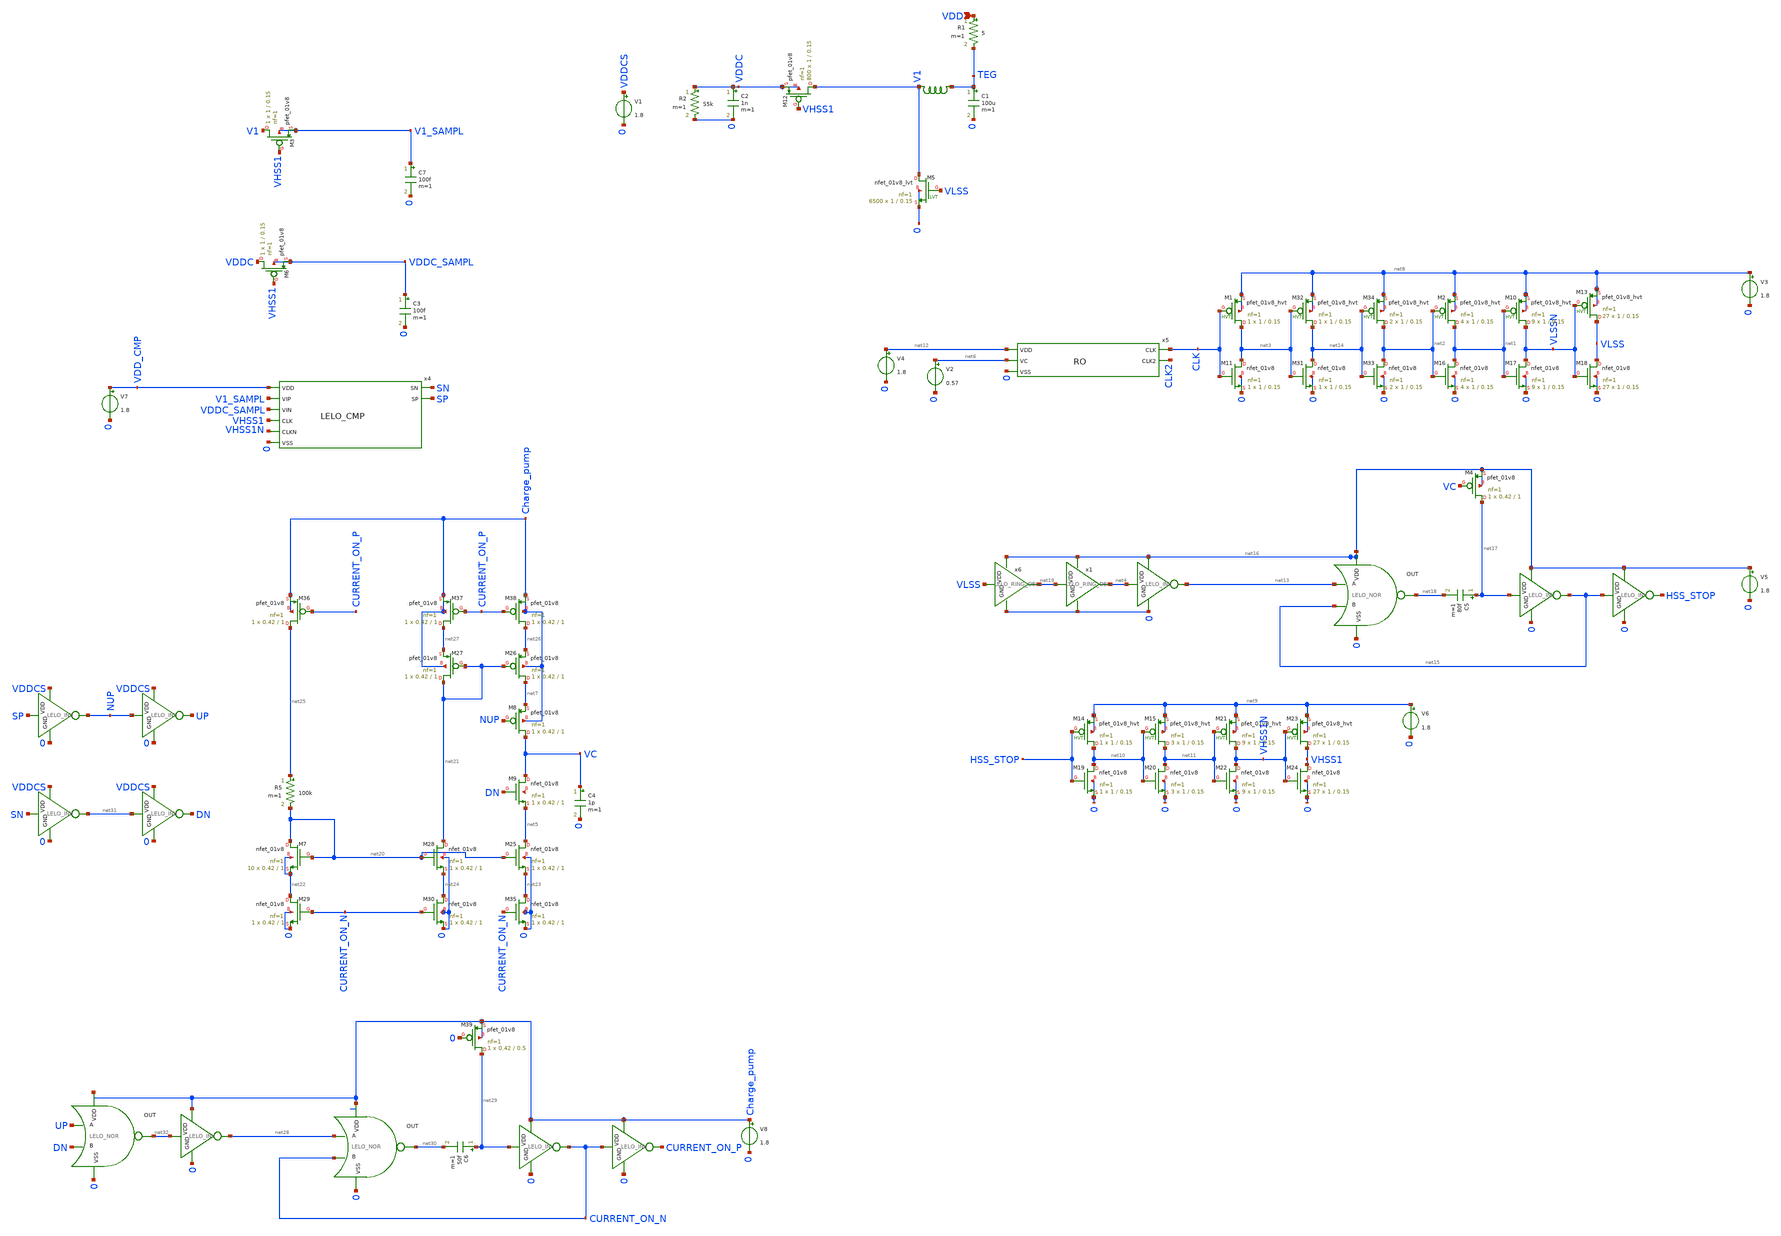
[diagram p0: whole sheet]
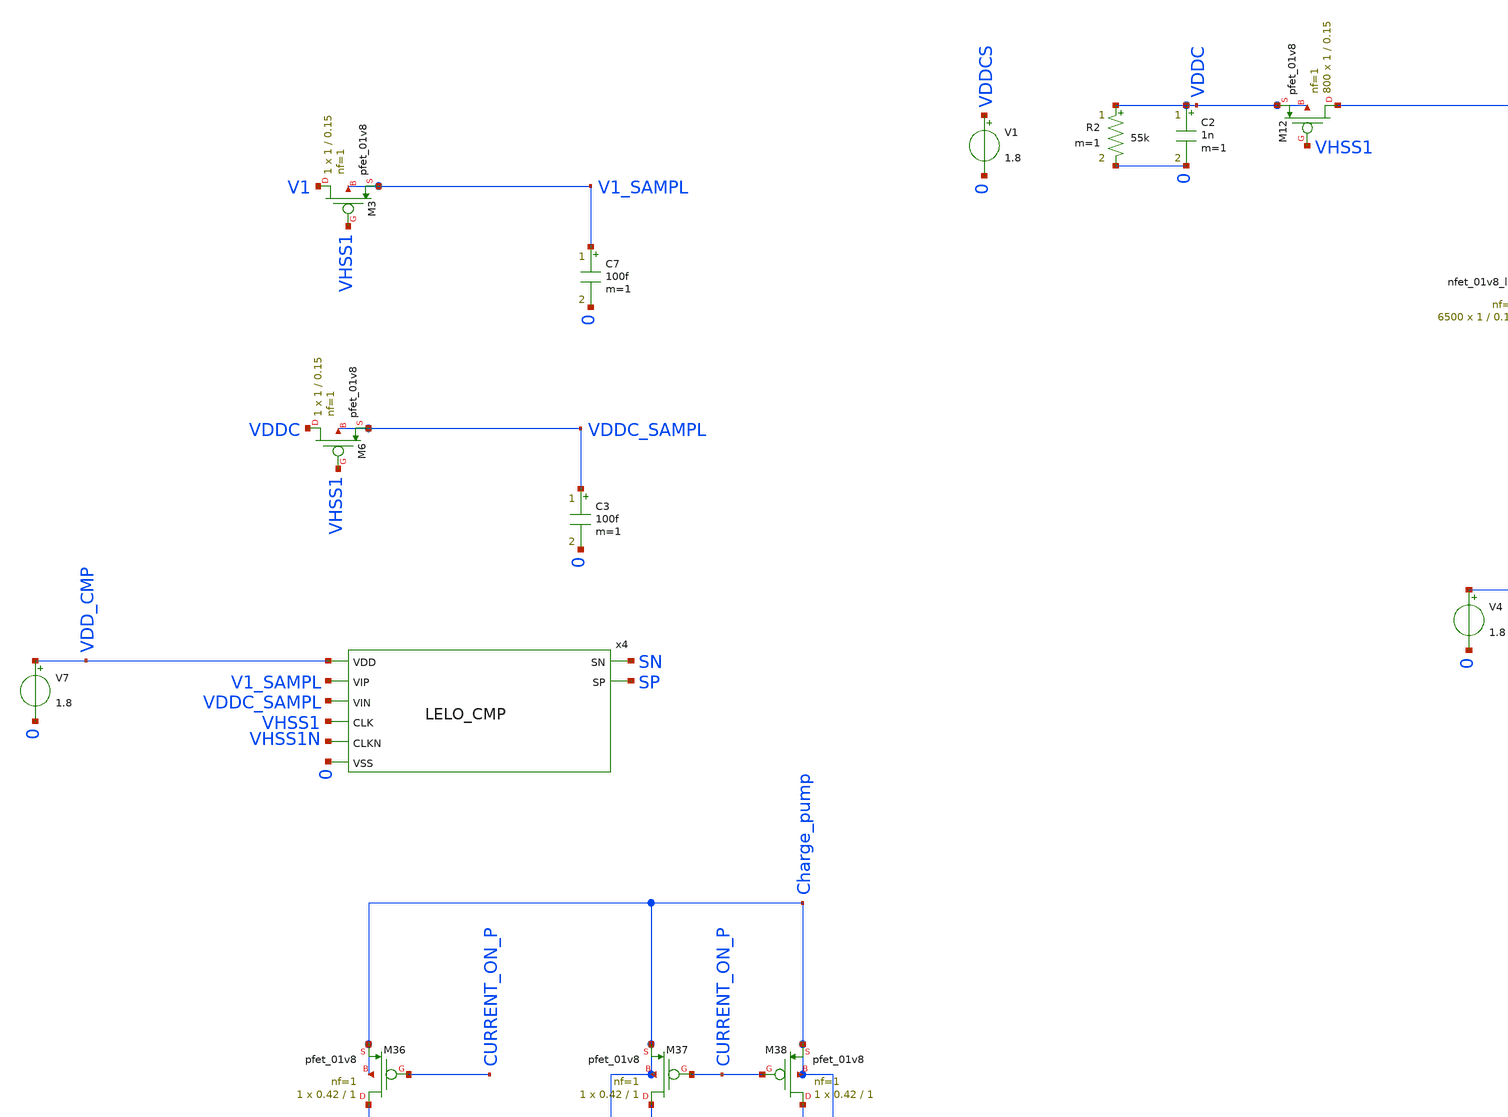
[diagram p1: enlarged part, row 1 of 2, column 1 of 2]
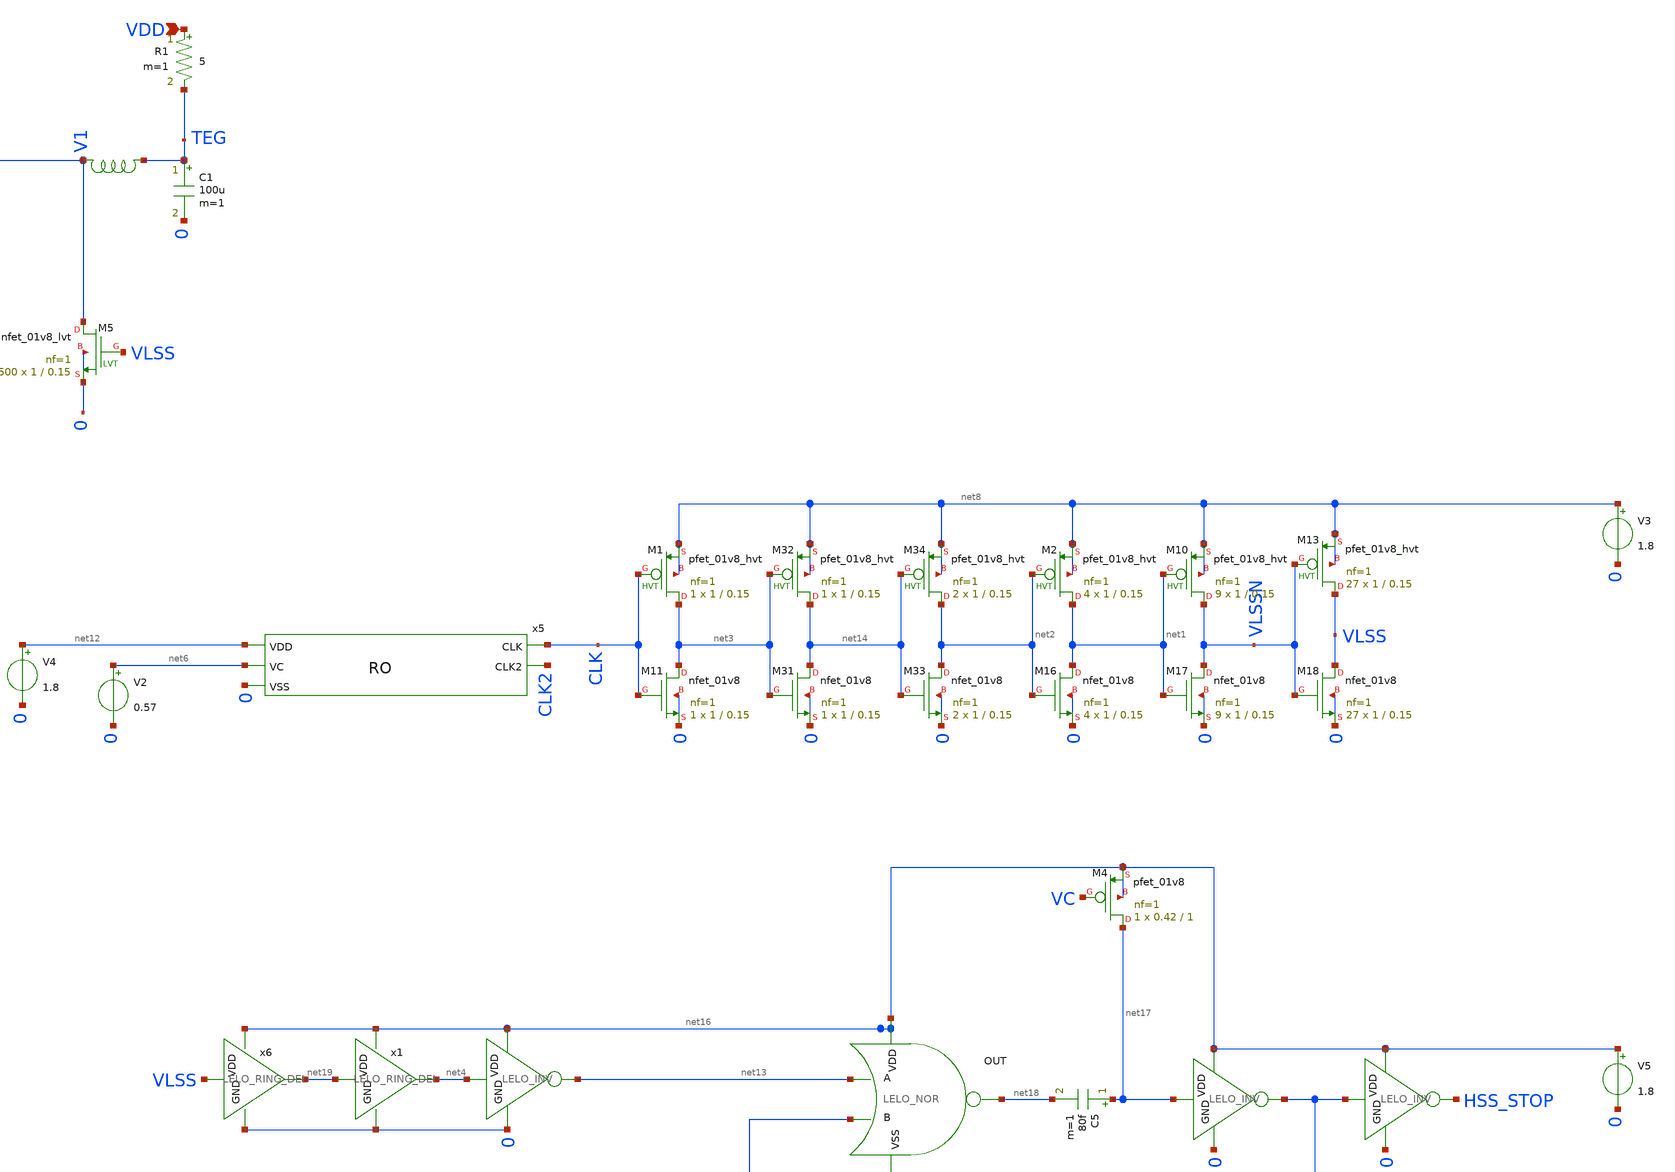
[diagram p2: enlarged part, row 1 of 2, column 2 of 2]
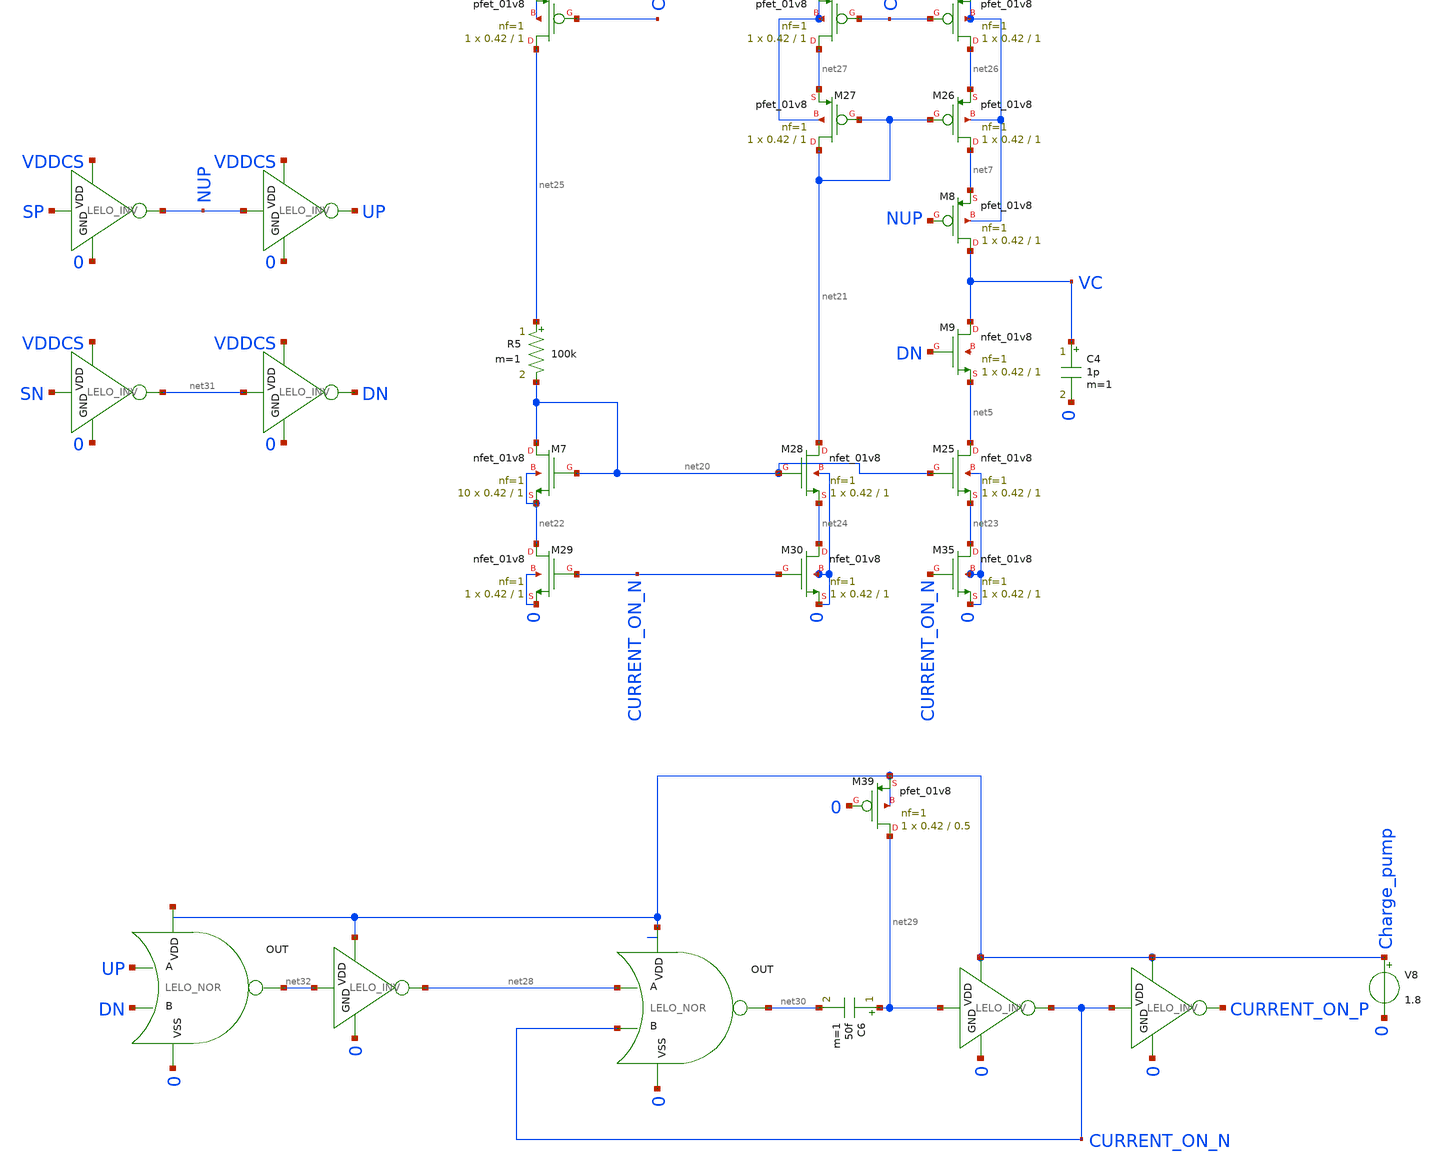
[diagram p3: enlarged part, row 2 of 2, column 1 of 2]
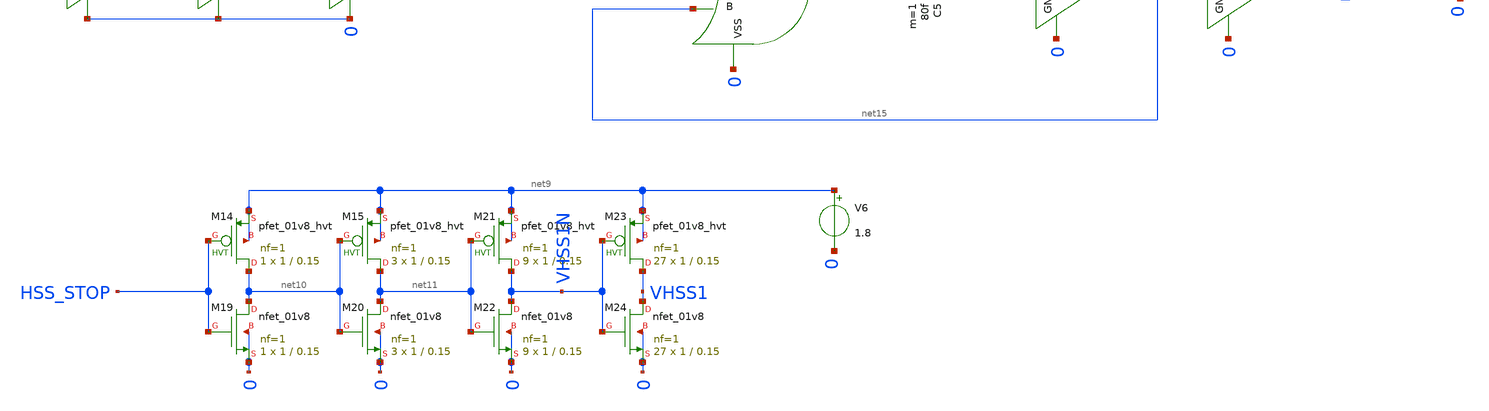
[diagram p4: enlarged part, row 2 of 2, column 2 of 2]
** sch_path: design/LELO_SVOD_SKY130A/LELO_BOOST_STEADY_STATE.sch
**.subckt LELO_BOOST_STEADY_STATE VDD
*.ipin VDD
R1 VDD TEG 5 m=1
C7 V1_SAMPL 0 100f m=1
x5 CLK CLK2 net12 net6 0 RO
XM12 V1 VHSS1 VDDC VDDC sky130_fd_pr__pfet_01v8 L=0.15 W=1 nf=1 ad='int((1 + 1)/2) * 1 / 1 * 0.29' as='int((1 + 2)/2) * 1 / 1 * 0.29'
+ pd='2*int((1 + 1)/2) * (1 / 1 + 0.29)' ps='2*int((1 + 2)/2) * (1 / 1 + 0.29)' nrd='0.29 / 1 ' nrs='0.29 / 1 '
+ sa=0 sb=0 sd=0 mult=800 m=800
x16 net16 net15 HSS_STOP 0 LELO_INV
C1 TEG 0 100u m=1
x9 net16 net4 net13 0 LELO_INV
XM5 V1 VLSS 0 0 sky130_fd_pr__nfet_01v8_lvt L=0.15 W=1 nf=1 ad='int((1 + 1)/2) * 1 / 1 * 0.29' as='int((1 + 2)/2) * 1 / 1 * 0.29'
+ pd='2*int((1 + 1)/2) * (1 / 1 + 0.29)' ps='2*int((1 + 2)/2) * (1 / 1 + 0.29)' nrd='0.29 / 1 ' nrs='0.29 / 1 '
+ sa=0 sb=0 sd=0 mult=6500 m=6500
C2 VDDC 0 1n m=1
V1 VDDCS 0 1.8
R2 VDDC 0 55k m=1
x4 SN SP VDD_CMP V1_SAMPL VDDC_SAMPL VHSS1 VHSS1N 0 LELO_CMP
XM3 V1 VHSS1 V1_SAMPL V1_SAMPL sky130_fd_pr__pfet_01v8 L=0.15 W=1 nf=1 ad='int((1 + 1)/2) * 1 / 1 * 0.29'
+ as='int((1 + 2)/2) * 1 / 1 * 0.29' pd='2*int((1 + 1)/2) * (1 / 1 + 0.29)' ps='2*int((1 + 2)/2) * (1 / 1 + 0.29)'
+ nrd='0.29 / 1 ' nrs='0.29 / 1 ' sa=0 sb=0 sd=0 mult=1 m=1
C3 VDDC_SAMPL 0 100f m=1
XM6 VDDC VHSS1 VDDC_SAMPL VDDC_SAMPL sky130_fd_pr__pfet_01v8 L=0.15 W=1 nf=1 ad='int((1 + 1)/2) * 1 / 1 * 0.29'
+ as='int((1 + 2)/2) * 1 / 1 * 0.29' pd='2*int((1 + 1)/2) * (1 / 1 + 0.29)' ps='2*int((1 + 2)/2) * (1 / 1 + 0.29)'
+ nrd='0.29 / 1 ' nrs='0.29 / 1 ' sa=0 sb=0 sd=0 mult=1 m=1
C4 VC 0 1p m=1
XM8 VC NUP net7 Charge_pump sky130_fd_pr__pfet_01v8 L=1 W=0.42 nf=1 ad='int((1 + 1)/2) * 0.42 / 1 * 0.29'
+ as='int((1 + 2)/2) * 0.42 / 1 * 0.29' pd='2*int((1 + 1)/2) * (0.42 / 1 + 0.29)' ps='2*int((1 + 2)/2) * (0.42 / 1 + 0.29)'
+ nrd='0.29 / 0.42 ' nrs='0.29 / 0.42 ' sa=0 sb=0 sd=0 mult=1 m=1
XM9 VC DN net5 net33 sky130_fd_pr__nfet_01v8 L=1 W=0.42 nf=1 ad='int((1 + 1)/2) * 0.42 / 1 * 0.29' as='int((1 + 2)/2) * 0.42 / 1 * 0.29'
+ pd='2*int((1 + 1)/2) * (0.42 / 1 + 0.29)' ps='2*int((1 + 2)/2) * (0.42 / 1 + 0.29)' nrd='0.29 / 0.42 '
+ nrs='0.29 / 0.42 ' sa=0 sb=0 sd=0 mult=1 m=1
V2 net6 0 0.57
XM11 net3 CLK 0 0 sky130_fd_pr__nfet_01v8 L=0.15 W=1 nf=1 ad='int((1 + 1)/2) * 1 / 1 * 0.29' as='int((1 + 2)/2) * 1 / 1 * 0.29'
+ pd='2*int((1 + 1)/2) * (1 / 1 + 0.29)' ps='2*int((1 + 2)/2) * (1 / 1 + 0.29)' nrd='0.29 / 1 ' nrs='0.29 / 1 '
+ sa=0 sb=0 sd=0 mult=1 m=1
XM16 net1 net2 0 0 sky130_fd_pr__nfet_01v8 L=0.15 W=1 nf=1 ad='int((1 + 1)/2) * 1 / 1 * 0.29' as='int((1 + 2)/2) * 1 / 1 * 0.29'
+ pd='2*int((1 + 1)/2) * (1 / 1 + 0.29)' ps='2*int((1 + 2)/2) * (1 / 1 + 0.29)' nrd='0.29 / 1 ' nrs='0.29 / 1 '
+ sa=0 sb=0 sd=0 mult=4 m=4
XM17 VLSSN net1 0 0 sky130_fd_pr__nfet_01v8 L=0.15 W=1 nf=1 ad='int((1 + 1)/2) * 1 / 1 * 0.29' as='int((1 + 2)/2) * 1 / 1 * 0.29'
+ pd='2*int((1 + 1)/2) * (1 / 1 + 0.29)' ps='2*int((1 + 2)/2) * (1 / 1 + 0.29)' nrd='0.29 / 1 ' nrs='0.29 / 1 '
+ sa=0 sb=0 sd=0 mult=9 m=9
XM18 VLSS VLSSN 0 0 sky130_fd_pr__nfet_01v8 L=0.15 W=1 nf=1 ad='int((1 + 1)/2) * 1 / 1 * 0.29' as='int((1 + 2)/2) * 1 / 1 * 0.29'
+ pd='2*int((1 + 1)/2) * (1 / 1 + 0.29)' ps='2*int((1 + 2)/2) * (1 / 1 + 0.29)' nrd='0.29 / 1 ' nrs='0.29 / 1 '
+ sa=0 sb=0 sd=0 mult=27 m=27
XM19 net10 HSS_STOP 0 0 sky130_fd_pr__nfet_01v8 L=0.15 W=1 nf=1 ad='int((1 + 1)/2) * 1 / 1 * 0.29' as='int((1 + 2)/2) * 1 / 1 * 0.29'
+ pd='2*int((1 + 1)/2) * (1 / 1 + 0.29)' ps='2*int((1 + 2)/2) * (1 / 1 + 0.29)' nrd='0.29 / 1 ' nrs='0.29 / 1 '
+ sa=0 sb=0 sd=0 mult=1 m=1
XM20 net11 net10 0 0 sky130_fd_pr__nfet_01v8 L=0.15 W=1 nf=1 ad='int((1 + 1)/2) * 1 / 1 * 0.29' as='int((1 + 2)/2) * 1 / 1 * 0.29'
+ pd='2*int((1 + 1)/2) * (1 / 1 + 0.29)' ps='2*int((1 + 2)/2) * (1 / 1 + 0.29)' nrd='0.29 / 1 ' nrs='0.29 / 1 '
+ sa=0 sb=0 sd=0 mult=3 m=3
XM22 VHSS1N net11 0 0 sky130_fd_pr__nfet_01v8 L=0.15 W=1 nf=1 ad='int((1 + 1)/2) * 1 / 1 * 0.29' as='int((1 + 2)/2) * 1 / 1 * 0.29'
+ pd='2*int((1 + 1)/2) * (1 / 1 + 0.29)' ps='2*int((1 + 2)/2) * (1 / 1 + 0.29)' nrd='0.29 / 1 ' nrs='0.29 / 1 '
+ sa=0 sb=0 sd=0 mult=9 m=9
XM24 VHSS1 VHSS1N 0 0 sky130_fd_pr__nfet_01v8 L=0.15 W=1 nf=1 ad='int((1 + 1)/2) * 1 / 1 * 0.29' as='int((1 + 2)/2) * 1 / 1 * 0.29'
+ pd='2*int((1 + 1)/2) * (1 / 1 + 0.29)' ps='2*int((1 + 2)/2) * (1 / 1 + 0.29)' nrd='0.29 / 1 ' nrs='0.29 / 1 '
+ sa=0 sb=0 sd=0 mult=27 m=27
XM1 net3 CLK net8 net8 sky130_fd_pr__pfet_01v8_hvt L=0.15 W=1 nf=1 ad='int((1 + 1)/2) * 1 / 1 * 0.29'
+ as='int((1 + 2)/2) * 1 / 1 * 0.29' pd='2*int((1 + 1)/2) * (1 / 1 + 0.29)' ps='2*int((1 + 2)/2) * (1 / 1 + 0.29)'
+ nrd='0.29 / 1 ' nrs='0.29 / 1 ' sa=0 sb=0 sd=0 mult=1 m=1
XM2 net1 net2 net8 net8 sky130_fd_pr__pfet_01v8_hvt L=0.15 W=1 nf=1 ad='int((1 + 1)/2) * 1 / 1 * 0.29'
+ as='int((1 + 2)/2) * 1 / 1 * 0.29' pd='2*int((1 + 1)/2) * (1 / 1 + 0.29)' ps='2*int((1 + 2)/2) * (1 / 1 + 0.29)'
+ nrd='0.29 / 1 ' nrs='0.29 / 1 ' sa=0 sb=0 sd=0 mult=4 m=4
XM10 VLSSN net1 net8 net8 sky130_fd_pr__pfet_01v8_hvt L=0.15 W=1 nf=1 ad='int((1 + 1)/2) * 1 / 1 * 0.29'
+ as='int((1 + 2)/2) * 1 / 1 * 0.29' pd='2*int((1 + 1)/2) * (1 / 1 + 0.29)' ps='2*int((1 + 2)/2) * (1 / 1 + 0.29)'
+ nrd='0.29 / 1 ' nrs='0.29 / 1 ' sa=0 sb=0 sd=0 mult=9 m=9
XM13 VLSS VLSSN net8 net8 sky130_fd_pr__pfet_01v8_hvt L=0.15 W=1 nf=1 ad='int((1 + 1)/2) * 1 / 1 * 0.29'
+ as='int((1 + 2)/2) * 1 / 1 * 0.29' pd='2*int((1 + 1)/2) * (1 / 1 + 0.29)' ps='2*int((1 + 2)/2) * (1 / 1 + 0.29)'
+ nrd='0.29 / 1 ' nrs='0.29 / 1 ' sa=0 sb=0 sd=0 mult=27 m=27
XM14 net10 HSS_STOP net9 net9 sky130_fd_pr__pfet_01v8_hvt L=0.15 W=1 nf=1 ad='int((1 + 1)/2) * 1 / 1 * 0.29'
+ as='int((1 + 2)/2) * 1 / 1 * 0.29' pd='2*int((1 + 1)/2) * (1 / 1 + 0.29)' ps='2*int((1 + 2)/2) * (1 / 1 + 0.29)'
+ nrd='0.29 / 1 ' nrs='0.29 / 1 ' sa=0 sb=0 sd=0 mult=1 m=1
XM15 net11 net10 net9 net9 sky130_fd_pr__pfet_01v8_hvt L=0.15 W=1 nf=1 ad='int((1 + 1)/2) * 1 / 1 * 0.29'
+ as='int((1 + 2)/2) * 1 / 1 * 0.29' pd='2*int((1 + 1)/2) * (1 / 1 + 0.29)' ps='2*int((1 + 2)/2) * (1 / 1 + 0.29)'
+ nrd='0.29 / 1 ' nrs='0.29 / 1 ' sa=0 sb=0 sd=0 mult=3 m=3
XM21 VHSS1N net11 net9 net9 sky130_fd_pr__pfet_01v8_hvt L=0.15 W=1 nf=1 ad='int((1 + 1)/2) * 1 / 1 * 0.29'
+ as='int((1 + 2)/2) * 1 / 1 * 0.29' pd='2*int((1 + 1)/2) * (1 / 1 + 0.29)' ps='2*int((1 + 2)/2) * (1 / 1 + 0.29)'
+ nrd='0.29 / 1 ' nrs='0.29 / 1 ' sa=0 sb=0 sd=0 mult=9 m=9
XM23 VHSS1 VHSS1N net9 net9 sky130_fd_pr__pfet_01v8_hvt L=0.15 W=1 nf=1 ad='int((1 + 1)/2) * 1 / 1 * 0.29'
+ as='int((1 + 2)/2) * 1 / 1 * 0.29' pd='2*int((1 + 1)/2) * (1 / 1 + 0.29)' ps='2*int((1 + 2)/2) * (1 / 1 + 0.29)'
+ nrd='0.29 / 1 ' nrs='0.29 / 1 ' sa=0 sb=0 sd=0 mult=27 m=27
V4 net12 0 1.8
V3 net8 0 1.8
V5 net16 0 1.8
V6 net9 0 1.8
V7 VDD_CMP 0 1.8
XM31 net14 net3 0 0 sky130_fd_pr__nfet_01v8 L=0.15 W=1 nf=1 ad='int((1 + 1)/2) * 1 / 1 * 0.29' as='int((1 + 2)/2) * 1 / 1 * 0.29'
+ pd='2*int((1 + 1)/2) * (1 / 1 + 0.29)' ps='2*int((1 + 2)/2) * (1 / 1 + 0.29)' nrd='0.29 / 1 ' nrs='0.29 / 1 '
+ sa=0 sb=0 sd=0 mult=1 m=1
XM32 net14 net3 net8 net8 sky130_fd_pr__pfet_01v8_hvt L=0.15 W=1 nf=1 ad='int((1 + 1)/2) * 1 / 1 * 0.29'
+ as='int((1 + 2)/2) * 1 / 1 * 0.29' pd='2*int((1 + 1)/2) * (1 / 1 + 0.29)' ps='2*int((1 + 2)/2) * (1 / 1 + 0.29)'
+ nrd='0.29 / 1 ' nrs='0.29 / 1 ' sa=0 sb=0 sd=0 mult=1 m=1
XM33 net2 net14 0 0 sky130_fd_pr__nfet_01v8 L=0.15 W=1 nf=1 ad='int((1 + 1)/2) * 1 / 1 * 0.29' as='int((1 + 2)/2) * 1 / 1 * 0.29'
+ pd='2*int((1 + 1)/2) * (1 / 1 + 0.29)' ps='2*int((1 + 2)/2) * (1 / 1 + 0.29)' nrd='0.29 / 1 ' nrs='0.29 / 1 '
+ sa=0 sb=0 sd=0 mult=2 m=2
XM34 net2 net14 net8 net8 sky130_fd_pr__pfet_01v8_hvt L=0.15 W=1 nf=1 ad='int((1 + 1)/2) * 1 / 1 * 0.29'
+ as='int((1 + 2)/2) * 1 / 1 * 0.29' pd='2*int((1 + 1)/2) * (1 / 1 + 0.29)' ps='2*int((1 + 2)/2) * (1 / 1 + 0.29)'
+ nrd='0.29 / 1 ' nrs='0.29 / 1 ' sa=0 sb=0 sd=0 mult=2 m=2
x7 TEG V1 XGL6030-822_sat
x10 VDDCS SP NUP 0 LELO_INV
x2 net16 net18 net13 net15 0 LELO_NOR
C5 net17 net18 80f m=1
x3 net16 net17 net15 0 LELO_INV
XM4 net17 VC net16 net16 sky130_fd_pr__pfet_01v8 L=1 W=0.42 nf=1 ad='int((1 + 1)/2) * 0.42 / 1 * 0.29'
+ as='int((1 + 2)/2) * 0.42 / 1 * 0.29' pd='2*int((1 + 1)/2) * (0.42 / 1 + 0.29)' ps='2*int((1 + 2)/2) * (0.42 / 1 + 0.29)'
+ nrd='0.29 / 0.42 ' nrs='0.29 / 0.42 ' sa=0 sb=0 sd=0 mult=1 m=1
x1 net16 net19 net4 0 LELO_RING_DEL
x6 net16 VLSS net19 0 LELO_RING_DEL
R5 net25 net20 100k m=1
XM7 net20 net20 net22 net22 sky130_fd_pr__nfet_01v8 L=1 W=0.42 nf=1 ad='int((1 + 1)/2) * 0.42 / 1 * 0.29'
+ as='int((1 + 2)/2) * 0.42 / 1 * 0.29' pd='2*int((1 + 1)/2) * (0.42 / 1 + 0.29)' ps='2*int((1 + 2)/2) * (0.42 / 1 + 0.29)'
+ nrd='0.29 / 0.42 ' nrs='0.29 / 0.42 ' sa=0 sb=0 sd=0 mult=10 m=10
XM25 net5 net20 net23 0 sky130_fd_pr__nfet_01v8 L=1 W=0.42 nf=1 ad='int((1 + 1)/2) * 0.42 / 1 * 0.29'
+ as='int((1 + 2)/2) * 0.42 / 1 * 0.29' pd='2*int((1 + 1)/2) * (0.42 / 1 + 0.29)' ps='2*int((1 + 2)/2) * (0.42 / 1 + 0.29)'
+ nrd='0.29 / 0.42 ' nrs='0.29 / 0.42 ' sa=0 sb=0 sd=0 mult=1 m=1
XM26 net7 net21 net26 Charge_pump sky130_fd_pr__pfet_01v8 L=1 W=0.42 nf=1 ad='int((1 + 1)/2) * 0.42 / 1 * 0.29'
+ as='int((1 + 2)/2) * 0.42 / 1 * 0.29' pd='2*int((1 + 1)/2) * (0.42 / 1 + 0.29)' ps='2*int((1 + 2)/2) * (0.42 / 1 + 0.29)'
+ nrd='0.29 / 0.42 ' nrs='0.29 / 0.42 ' sa=0 sb=0 sd=0 mult=1 m=1
XM27 net21 net21 net27 Charge_pump sky130_fd_pr__pfet_01v8 L=1 W=0.42 nf=1 ad='int((1 + 1)/2) * 0.42 / 1 * 0.29'
+ as='int((1 + 2)/2) * 0.42 / 1 * 0.29' pd='2*int((1 + 1)/2) * (0.42 / 1 + 0.29)' ps='2*int((1 + 2)/2) * (0.42 / 1 + 0.29)'
+ nrd='0.29 / 0.42 ' nrs='0.29 / 0.42 ' sa=0 sb=0 sd=0 mult=1 m=1
XM28 net21 net20 net24 0 sky130_fd_pr__nfet_01v8 L=1 W=0.42 nf=1 ad='int((1 + 1)/2) * 0.42 / 1 * 0.29'
+ as='int((1 + 2)/2) * 0.42 / 1 * 0.29' pd='2*int((1 + 1)/2) * (0.42 / 1 + 0.29)' ps='2*int((1 + 2)/2) * (0.42 / 1 + 0.29)'
+ nrd='0.29 / 0.42 ' nrs='0.29 / 0.42 ' sa=0 sb=0 sd=0 mult=1 m=1
XM29 net22 CURRENT_ON_N 0 0 sky130_fd_pr__nfet_01v8 L=1 W=0.42 nf=1 ad='int((1 + 1)/2) * 0.42 / 1 * 0.29'
+ as='int((1 + 2)/2) * 0.42 / 1 * 0.29' pd='2*int((1 + 1)/2) * (0.42 / 1 + 0.29)' ps='2*int((1 + 2)/2) * (0.42 / 1 + 0.29)'
+ nrd='0.29 / 0.42 ' nrs='0.29 / 0.42 ' sa=0 sb=0 sd=0 mult=1 m=1
XM30 net24 CURRENT_ON_N 0 0 sky130_fd_pr__nfet_01v8 L=1 W=0.42 nf=1 ad='int((1 + 1)/2) * 0.42 / 1 * 0.29'
+ as='int((1 + 2)/2) * 0.42 / 1 * 0.29' pd='2*int((1 + 1)/2) * (0.42 / 1 + 0.29)' ps='2*int((1 + 2)/2) * (0.42 / 1 + 0.29)'
+ nrd='0.29 / 0.42 ' nrs='0.29 / 0.42 ' sa=0 sb=0 sd=0 mult=1 m=1
XM35 net23 CURRENT_ON_N 0 0 sky130_fd_pr__nfet_01v8 L=1 W=0.42 nf=1 ad='int((1 + 1)/2) * 0.42 / 1 * 0.29'
+ as='int((1 + 2)/2) * 0.42 / 1 * 0.29' pd='2*int((1 + 1)/2) * (0.42 / 1 + 0.29)' ps='2*int((1 + 2)/2) * (0.42 / 1 + 0.29)'
+ nrd='0.29 / 0.42 ' nrs='0.29 / 0.42 ' sa=0 sb=0 sd=0 mult=1 m=1
XM36 net25 CURRENT_ON_P Charge_pump Charge_pump sky130_fd_pr__pfet_01v8 L=1 W=0.42 nf=1 ad='int((1 + 1)/2) * 0.42 / 1 * 0.29'
+ as='int((1 + 2)/2) * 0.42 / 1 * 0.29' pd='2*int((1 + 1)/2) * (0.42 / 1 + 0.29)' ps='2*int((1 + 2)/2) * (0.42 / 1 + 0.29)'
+ nrd='0.29 / 0.42 ' nrs='0.29 / 0.42 ' sa=0 sb=0 sd=0 mult=1 m=1
XM37 net27 CURRENT_ON_P Charge_pump Charge_pump sky130_fd_pr__pfet_01v8 L=1 W=0.42 nf=1 ad='int((1 + 1)/2) * 0.42 / 1 * 0.29'
+ as='int((1 + 2)/2) * 0.42 / 1 * 0.29' pd='2*int((1 + 1)/2) * (0.42 / 1 + 0.29)' ps='2*int((1 + 2)/2) * (0.42 / 1 + 0.29)'
+ nrd='0.29 / 0.42 ' nrs='0.29 / 0.42 ' sa=0 sb=0 sd=0 mult=1 m=1
XM38 net26 CURRENT_ON_P Charge_pump Charge_pump sky130_fd_pr__pfet_01v8 L=1 W=0.42 nf=1 ad='int((1 + 1)/2) * 0.42 / 1 * 0.29'
+ as='int((1 + 2)/2) * 0.42 / 1 * 0.29' pd='2*int((1 + 1)/2) * (0.42 / 1 + 0.29)' ps='2*int((1 + 2)/2) * (0.42 / 1 + 0.29)'
+ nrd='0.29 / 0.42 ' nrs='0.29 / 0.42 ' sa=0 sb=0 sd=0 mult=1 m=1
x8 Charge_pump CURRENT_ON_N CURRENT_ON_P 0 LELO_INV
V8 Charge_pump 0 1.8
x12 Charge_pump net30 net28 CURRENT_ON_N 0 LELO_NOR
C6 net29 net30 50f m=1
x13 Charge_pump net29 CURRENT_ON_N 0 LELO_INV
XM39 net29 0 Charge_pump Charge_pump sky130_fd_pr__pfet_01v8 L=0.5 W=0.42 nf=1 ad='int((1 + 1)/2) * 0.42 / 1 * 0.29'
+ as='int((1 + 2)/2) * 0.42 / 1 * 0.29' pd='2*int((1 + 1)/2) * (0.42 / 1 + 0.29)' ps='2*int((1 + 2)/2) * (0.42 / 1 + 0.29)'
+ nrd='0.29 / 0.42 ' nrs='0.29 / 0.42 ' sa=0 sb=0 sd=0 mult=1 m=1
x11 VDDCS SN net31 0 LELO_INV
x14 VDDCS net31 DN 0 LELO_INV
x15 net34 net32 UP DN 0 LELO_NOR
x17 VDDCS NUP UP 0 LELO_INV
x18 Charge_pump net32 net28 0 LELO_INV
**.ends

* expanding   symbol:  LELO_SVOD_SKY130A/RO.sym # of pins=5
** sym_path: design/LELO_SVOD_SKY130A/RO.sym
** sch_path: design/LELO_SVOD_SKY130A/RO.sch
.subckt RO CLK CLK2 VDD VC VSS
*.opin CLK
*.ipin VSS
*.opin CLK2
*.ipin VDD
*.ipin VC
x1 VDD VC2 CLK net1 VC VSS LELO_RING_DEL_VC
x2 VDD VC2 net1 net2 VC VSS LELO_RING_DEL_VC
x3 VDD VC2 net2 net3 VC VSS LELO_RING_DEL_VC
x4 VDD VC2 net3 CLK2 VC VSS LELO_RING_DEL_VC
x5 VDD VC2 CLK2 net4 VC VSS LELO_RING_DEL_VC
x6 VDD VC2 net4 net5 VC VSS LELO_RING_DEL_VC
x7 VDD VC2 net5 CLK VC VSS LELO_RING_DEL_VC
XM1 VC2 VC VSS VSS sky130_fd_pr__nfet_01v8 L=5 W=0.42 nf=1 ad='int((1 + 1)/2) * 0.42 / 1 * 0.29' as='int((1 + 2)/2) * 0.42 / 1 * 0.29'
+ pd='2*int((1 + 1)/2) * (0.42 / 1 + 0.29)' ps='2*int((1 + 2)/2) * (0.42 / 1 + 0.29)' nrd='0.29 / 0.42 '
+ nrs='0.29 / 0.42 ' sa=0 sb=0 sd=0 mult=1 m=1
XM2 VC2 VC2 VDD VDD sky130_fd_pr__pfet_01v8 L=5 W=0.42 nf=1 ad='int((1 + 1)/2) * 0.42 / 1 * 0.29' as='int((1 + 2)/2) * 0.42 / 1 * 0.29'
+ pd='2*int((1 + 1)/2) * (0.42 / 1 + 0.29)' ps='2*int((1 + 2)/2) * (0.42 / 1 + 0.29)' nrd='0.29 / 0.42 '
+ nrs='0.29 / 0.42 ' sa=0 sb=0 sd=0 mult=1 m=1
.ends


* expanding   symbol:  LELO_SVOD_SKY130A/LELO_INV.sym # of pins=4
** sym_path: design/LELO_SVOD_SKY130A/LELO_INV.sym
** sch_path: design/LELO_SVOD_SKY130A/LELO_INV.sch
.subckt LELO_INV VDD VIN VOUT GND
*.ipin VIN
*.ipin VDD
*.ipin GND
*.opin VOUT
XM1 VOUT VIN GND GND sky130_fd_pr__nfet_01v8_lvt L=0.15 W=1 nf=1 ad='int((1 + 1)/2) * 1 / 1 * 0.29' as='int((1 + 2)/2) * 1 / 1 * 0.29'
+ pd='2*int((1 + 1)/2) * (1 / 1 + 0.29)' ps='2*int((1 + 2)/2) * (1 / 1 + 0.29)' nrd='0.29 / 1 ' nrs='0.29 / 1 '
+ sa=0 sb=0 sd=0 mult=1 m=1
XM2 VOUT VIN VDD VDD sky130_fd_pr__pfet_01v8_lvt L=0.35 W=1 nf=1 ad='int((1 + 1)/2) * 1 / 1 * 0.29' as='int((1 + 2)/2) * 1 / 1 * 0.29'
+ pd='2*int((1 + 1)/2) * (1 / 1 + 0.29)' ps='2*int((1 + 2)/2) * (1 / 1 + 0.29)' nrd='0.29 / 1 ' nrs='0.29 / 1 '
+ sa=0 sb=0 sd=0 mult=2 m=2
.ends


* expanding   symbol:  LELO_SVOD_SKY130A/LELO_CMP.sym # of pins=8
** sym_path: design/LELO_SVOD_SKY130A/LELO_CMP.sym
** sch_path: design/LELO_SVOD_SKY130A/LELO_CMP.sch
.subckt LELO_CMP SN SP VDD VIP VIN CLK CLKN VSS
*.ipin VIP
*.ipin VIN
*.ipin CLK
*.ipin CLKN
*.ipin VDD
*.ipin VSS
*.opin SN
*.opin SP
XM2 SN net3 net5 VDD sky130_fd_pr__pfet_01v8_lvt L=0.44 W=1.92 nf=2 ad='int((2 + 1)/2) * 1.92 / 2 * 0.29'
+ as='int((2 + 2)/2) * 1.92 / 2 * 0.29' pd='2*int((2 + 1)/2) * (1.92 / 2 + 0.29)' ps='2*int((2 + 2)/2) * (1.92 / 2 + 0.29)'
+ nrd='0.29 / 1.92 ' nrs='0.29 / 1.92 ' sa=0 sb=0 sd=0 mult=3 m=3
XM1 SP net2 net6 VDD sky130_fd_pr__pfet_01v8_lvt L=0.44 W=1.92 nf=2 ad='int((2 + 1)/2) * 1.92 / 2 * 0.29'
+ as='int((2 + 2)/2) * 1.92 / 2 * 0.29' pd='2*int((2 + 1)/2) * (1.92 / 2 + 0.29)' ps='2*int((2 + 2)/2) * (1.92 / 2 + 0.29)'
+ nrd='0.29 / 1.92 ' nrs='0.29 / 1.92 ' sa=0 sb=0 sd=0 mult=3 m=3
XM3 net2 VIP net1 VSS sky130_fd_pr__nfet_01v8_lvt L=0.44 W=6.4 nf=1 ad='int((1 + 1)/2) * 6.4 / 1 * 0.29'
+ as='int((1 + 2)/2) * 6.4 / 1 * 0.29' pd='2*int((1 + 1)/2) * (6.4 / 1 + 0.29)' ps='2*int((1 + 2)/2) * (6.4 / 1 + 0.29)'
+ nrd='0.29 / 6.4 ' nrs='0.29 / 6.4 ' sa=0 sb=0 sd=0 mult=1 m=1
XM4 net3 VIN net1 VSS sky130_fd_pr__nfet_01v8_lvt L=0.44 W=6.4 nf=1 ad='int((1 + 1)/2) * 6.4 / 1 * 0.29'
+ as='int((1 + 2)/2) * 6.4 / 1 * 0.29' pd='2*int((1 + 1)/2) * (6.4 / 1 + 0.29)' ps='2*int((1 + 2)/2) * (6.4 / 1 + 0.29)'
+ nrd='0.29 / 6.4 ' nrs='0.29 / 6.4 ' sa=0 sb=0 sd=0 mult=1 m=1
XM5 net3 CLK VDD VDD sky130_fd_pr__pfet_01v8_lvt L=0.94 W=1.92 nf=2 ad='int((2 + 1)/2) * 1.92 / 2 * 0.29'
+ as='int((2 + 2)/2) * 1.92 / 2 * 0.29' pd='2*int((2 + 1)/2) * (1.92 / 2 + 0.29)' ps='2*int((2 + 2)/2) * (1.92 / 2 + 0.29)'
+ nrd='0.29 / 1.92 ' nrs='0.29 / 1.92 ' sa=0 sb=0 sd=0 mult=1 m=1
XM6 net6 SN VDD VDD sky130_fd_pr__pfet_01v8_lvt L=0.94 W=1.92 nf=2 ad='int((2 + 1)/2) * 1.92 / 2 * 0.29'
+ as='int((2 + 2)/2) * 1.92 / 2 * 0.29' pd='2*int((2 + 1)/2) * (1.92 / 2 + 0.29)' ps='2*int((2 + 2)/2) * (1.92 / 2 + 0.29)'
+ nrd='0.29 / 1.92 ' nrs='0.29 / 1.92 ' sa=0 sb=0 sd=0 mult=1 m=1
XM7 net5 SP VDD VDD sky130_fd_pr__pfet_01v8_lvt L=0.94 W=1.92 nf=2 ad='int((2 + 1)/2) * 1.92 / 2 * 0.29'
+ as='int((2 + 2)/2) * 1.92 / 2 * 0.29' pd='2*int((2 + 1)/2) * (1.92 / 2 + 0.29)' ps='2*int((2 + 2)/2) * (1.92 / 2 + 0.29)'
+ nrd='0.29 / 1.92 ' nrs='0.29 / 1.92 ' sa=0 sb=0 sd=0 mult=1 m=1
XM8 net2 CLK VDD VDD sky130_fd_pr__pfet_01v8_lvt L=0.94 W=1.92 nf=2 ad='int((2 + 1)/2) * 1.92 / 2 * 0.29'
+ as='int((2 + 2)/2) * 1.92 / 2 * 0.29' pd='2*int((2 + 1)/2) * (1.92 / 2 + 0.29)' ps='2*int((2 + 2)/2) * (1.92 / 2 + 0.29)'
+ nrd='0.29 / 1.92 ' nrs='0.29 / 1.92 ' sa=0 sb=0 sd=0 mult=1 m=1
XM9 net1 CLK net4 VSS sky130_fd_pr__nfet_01v8 L=0.94 W=1.92 nf=2 ad='int((2 + 1)/2) * 1.92 / 2 * 0.29'
+ as='int((2 + 2)/2) * 1.92 / 2 * 0.29' pd='2*int((2 + 1)/2) * (1.92 / 2 + 0.29)' ps='2*int((2 + 2)/2) * (1.92 / 2 + 0.29)'
+ nrd='0.29 / 1.92 ' nrs='0.29 / 1.92 ' sa=0 sb=0 sd=0 mult=1 m=1
XM10 net4 CLK VSS VSS sky130_fd_pr__nfet_01v8 L=0.94 W=1.92 nf=2 ad='int((2 + 1)/2) * 1.92 / 2 * 0.29'
+ as='int((2 + 2)/2) * 1.92 / 2 * 0.29' pd='2*int((2 + 1)/2) * (1.92 / 2 + 0.29)' ps='2*int((2 + 2)/2) * (1.92 / 2 + 0.29)'
+ nrd='0.29 / 1.92 ' nrs='0.29 / 1.92 ' sa=0 sb=0 sd=0 mult=1 m=1
XM11 SN CLKN VSS VSS sky130_fd_pr__nfet_01v8 L=0.94 W=1.92 nf=2 ad='int((2 + 1)/2) * 1.92 / 2 * 0.29'
+ as='int((2 + 2)/2) * 1.92 / 2 * 0.29' pd='2*int((2 + 1)/2) * (1.92 / 2 + 0.29)' ps='2*int((2 + 2)/2) * (1.92 / 2 + 0.29)'
+ nrd='0.29 / 1.92 ' nrs='0.29 / 1.92 ' sa=0 sb=0 sd=0 mult=1 m=1
XM12 SP SN VSS VSS sky130_fd_pr__nfet_01v8 L=0.94 W=1.92 nf=2 ad='int((2 + 1)/2) * 1.92 / 2 * 0.29' as='int((2 + 2)/2) * 1.92 / 2 * 0.29'
+ pd='2*int((2 + 1)/2) * (1.92 / 2 + 0.29)' ps='2*int((2 + 2)/2) * (1.92 / 2 + 0.29)' nrd='0.29 / 1.92 '
+ nrs='0.29 / 1.92 ' sa=0 sb=0 sd=0 mult=1 m=1
XM13 SN SP VSS VSS sky130_fd_pr__nfet_01v8 L=0.94 W=1.92 nf=2 ad='int((2 + 1)/2) * 1.92 / 2 * 0.29' as='int((2 + 2)/2) * 1.92 / 2 * 0.29'
+ pd='2*int((2 + 1)/2) * (1.92 / 2 + 0.29)' ps='2*int((2 + 2)/2) * (1.92 / 2 + 0.29)' nrd='0.29 / 1.92 '
+ nrs='0.29 / 1.92 ' sa=0 sb=0 sd=0 mult=1 m=1
XM14 SP CLKN VSS VSS sky130_fd_pr__nfet_01v8 L=0.94 W=1.92 nf=2 ad='int((2 + 1)/2) * 1.92 / 2 * 0.29'
+ as='int((2 + 2)/2) * 1.92 / 2 * 0.29' pd='2*int((2 + 1)/2) * (1.92 / 2 + 0.29)' ps='2*int((2 + 2)/2) * (1.92 / 2 + 0.29)'
+ nrd='0.29 / 1.92 ' nrs='0.29 / 1.92 ' sa=0 sb=0 sd=0 mult=1 m=1
.ends


* expanding   symbol:  LELO_SVOD_SKY130A/XGL6030-822_sat.sym # of pins=2
** sym_path: design/LELO_SVOD_SKY130A/XGL6030-822_sat.sym

.subckt XGL6030-822_sat port1 port2
X1 port1 port2 Model1C R1=5 R2=0.04 C= 15.2p K1=0.000001 K2=2 K3= 8.2u K4=0.000001 K5=0.000001
+ L=8.1093E-06 Is=13.9236 a=0.7109 L_Z0=0 L_EL=0 L_F0=0E6 PkZ=7057.14402
.ends XGL6030-822_sat


* expanding   symbol:  LELO_SVOD_SKY130A/LELO_NOR.sym # of pins=5
** sym_path: design/LELO_SVOD_SKY130A/LELO_NOR.sym
** sch_path: design/LELO_SVOD_SKY130A/LELO_NOR.sch
.subckt LELO_NOR VDD OUT A B VSS
*.ipin VDD
*.ipin VSS
*.opin OUT
*.ipin A
*.ipin B
XM2 OUT B VSS VSS sky130_fd_pr__nfet_01v8 L=0.15 W=2 nf=1 ad='int((1 + 1)/2) * 2 / 1 * 0.29' as='int((1 + 2)/2) * 2 / 1 * 0.29'
+ pd='2*int((1 + 1)/2) * (2 / 1 + 0.29)' ps='2*int((1 + 2)/2) * (2 / 1 + 0.29)' nrd='0.29 / 2 ' nrs='0.29 / 2 '
+ sa=0 sb=0 sd=0 mult=1 m=1
XM1 OUT A VSS VSS sky130_fd_pr__nfet_01v8 L=0.15 W=2 nf=1 ad='int((1 + 1)/2) * 2 / 1 * 0.29' as='int((1 + 2)/2) * 2 / 1 * 0.29'
+ pd='2*int((1 + 1)/2) * (2 / 1 + 0.29)' ps='2*int((1 + 2)/2) * (2 / 1 + 0.29)' nrd='0.29 / 2 ' nrs='0.29 / 2 '
+ sa=0 sb=0 sd=0 mult=1 m=1
XM3 OUT B net1 VDD sky130_fd_pr__pfet_01v8 L=0.15 W=4 nf=1 ad='int((1 + 1)/2) * 4 / 1 * 0.29' as='int((1 + 2)/2) * 4 / 1 * 0.29'
+ pd='2*int((1 + 1)/2) * (4 / 1 + 0.29)' ps='2*int((1 + 2)/2) * (4 / 1 + 0.29)' nrd='0.29 / 4 ' nrs='0.29 / 4 '
+ sa=0 sb=0 sd=0 mult=1 m=1
XM4 net1 A VDD VDD sky130_fd_pr__pfet_01v8 L=0.15 W=4 nf=1 ad='int((1 + 1)/2) * 4 / 1 * 0.29' as='int((1 + 2)/2) * 4 / 1 * 0.29'
+ pd='2*int((1 + 1)/2) * (4 / 1 + 0.29)' ps='2*int((1 + 2)/2) * (4 / 1 + 0.29)' nrd='0.29 / 4 ' nrs='0.29 / 4 '
+ sa=0 sb=0 sd=0 mult=1 m=1
.ends


* expanding   symbol:  LELO_SVOD_SKY130A/LELO_RING_DEL.sym # of pins=4
** sym_path: design/LELO_SVOD_SKY130A/LELO_RING_DEL.sym
** sch_path: design/LELO_SVOD_SKY130A/LELO_RING_DEL.sch
.subckt LELO_RING_DEL VDD VIN VOUT GND
*.ipin VIN
*.ipin VDD
*.ipin GND
*.opin VOUT
XM1 VOUT VIN VDD VDD sky130_fd_pr__pfet_01v8_hvt L=1.7 W=0.42 nf=1 ad='int((1 + 1)/2) * 0.42 / 1 * 0.29'
+ as='int((1 + 2)/2) * 0.42 / 1 * 0.29' pd='2*int((1 + 1)/2) * (0.42 / 1 + 0.29)' ps='2*int((1 + 2)/2) * (0.42 / 1 + 0.29)'
+ nrd='0.29 / 0.42 ' nrs='0.29 / 0.42 ' sa=0 sb=0 sd=0 mult=1 m=1
XM2 VOUT VIN GND GND sky130_fd_pr__nfet_01v8 L=1.7 W=0.42 nf=1 ad='int((1 + 1)/2) * 0.42 / 1 * 0.29'
+ as='int((1 + 2)/2) * 0.42 / 1 * 0.29' pd='2*int((1 + 1)/2) * (0.42 / 1 + 0.29)' ps='2*int((1 + 2)/2) * (0.42 / 1 + 0.29)'
+ nrd='0.29 / 0.42 ' nrs='0.29 / 0.42 ' sa=0 sb=0 sd=0 mult=1 m=1
.ends


* expanding   symbol:  LELO_SVOD_SKY130A/LELO_RING_DEL_VC.sym # of pins=6
** sym_path: design/LELO_SVOD_SKY130A/LELO_RING_DEL_VC.sym
** sch_path: design/LELO_SVOD_SKY130A/LELO_RING_DEL_VC.sch
.subckt LELO_RING_DEL_VC VDD VC2 VIN VOUT VC GND
*.ipin VIN
*.ipin VDD
*.ipin GND
*.opin VOUT
*.ipin VC
*.ipin VC2
XM3 VOUT VIN net1 GND sky130_fd_pr__nfet_01v8 L=1 W=0.42 nf=1 ad='int((1 + 1)/2) * 0.42 / 1 * 0.29' as='int((1 + 2)/2) * 0.42 / 1 * 0.29'
+ pd='2*int((1 + 1)/2) * (0.42 / 1 + 0.29)' ps='2*int((1 + 2)/2) * (0.42 / 1 + 0.29)' nrd='0.29 / 0.42 '
+ nrs='0.29 / 0.42 ' sa=0 sb=0 sd=0 mult=1 m=1
XM4 net1 VC GND GND sky130_fd_pr__nfet_01v8 L=4 W=0.42 nf=1 ad='int((1 + 1)/2) * 0.42 / 1 * 0.29' as='int((1 + 2)/2) * 0.42 / 1 * 0.29'
+ pd='2*int((1 + 1)/2) * (0.42 / 1 + 0.29)' ps='2*int((1 + 2)/2) * (0.42 / 1 + 0.29)' nrd='0.29 / 0.42 '
+ nrs='0.29 / 0.42 ' sa=0 sb=0 sd=0 mult=1 m=1
XM1 net2 VC2 VDD VDD sky130_fd_pr__pfet_01v8_lvt L=4 W=0.42 nf=1 ad='int((1 + 1)/2) * 0.42 / 1 * 0.29'
+ as='int((1 + 2)/2) * 0.42 / 1 * 0.29' pd='2*int((1 + 1)/2) * (0.42 / 1 + 0.29)' ps='2*int((1 + 2)/2) * (0.42 / 1 + 0.29)'
+ nrd='0.29 / 0.42 ' nrs='0.29 / 0.42 ' sa=0 sb=0 sd=0 mult=1 m=1
XM2 VOUT VIN net2 VDD sky130_fd_pr__pfet_01v8_lvt L=0.35 W=1 nf=1 ad='int((1 + 1)/2) * 1 / 1 * 0.29'
+ as='int((1 + 2)/2) * 1 / 1 * 0.29' pd='2*int((1 + 1)/2) * (1 / 1 + 0.29)' ps='2*int((1 + 2)/2) * (1 / 1 + 0.29)'
+ nrd='0.29 / 1 ' nrs='0.29 / 1 ' sa=0 sb=0 sd=0 mult=1 m=1
.ends

.end
